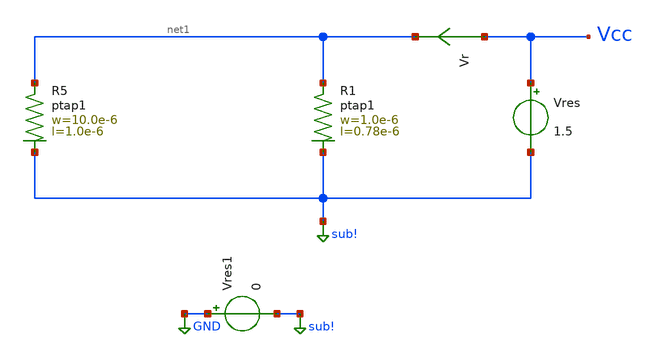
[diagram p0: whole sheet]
** sch_path: ihp-sg13g2/xschem_libs/sg13g2_tests_ase/dc_ptap1/schematic/dc_ptap1.sch
* Copyright 2023 IHP PDK Authors
**.subckt dc_ptap1
Vres Vcc sub! 1.5
Vr Vcc net1 0
.save i(vr)
XR5 net1 sub! ptap1 R=30.62 w=10.0e-6 l=1.0e-6
XR1 net1 sub! ptap1 R=225.8 w=1.0e-6 l=0.78e-6
Vres1 GND sub! 0
**.ends
.GLOBAL GND
.GLOBAL sub!
.end
